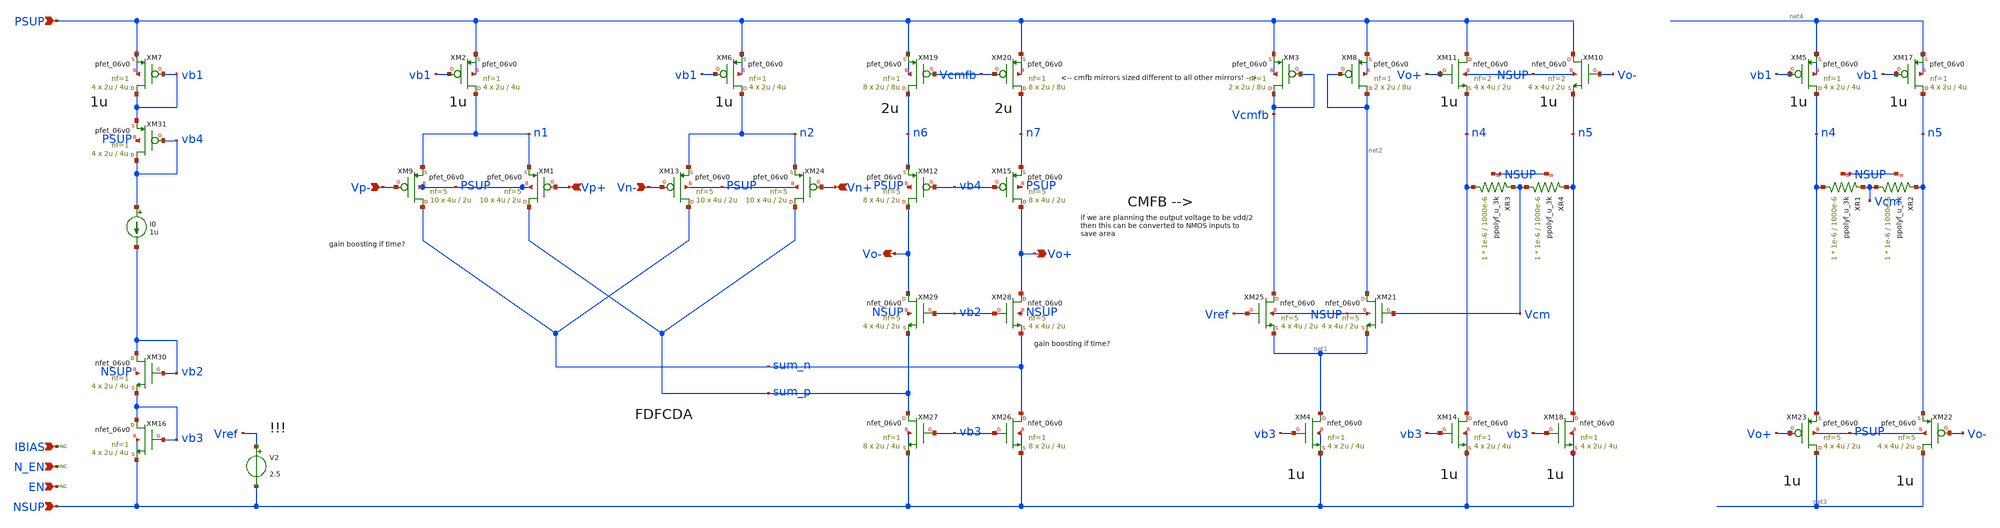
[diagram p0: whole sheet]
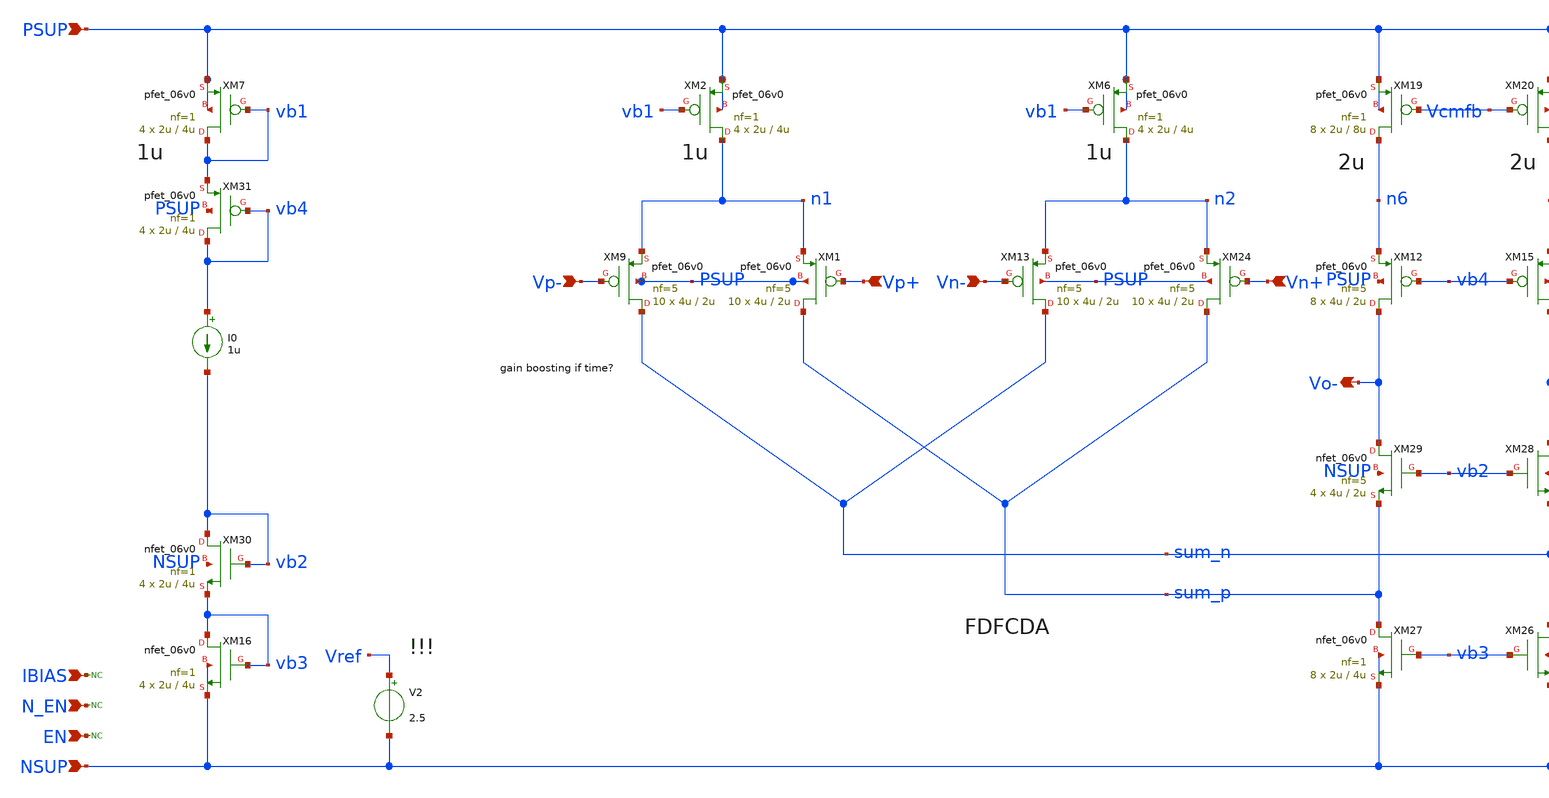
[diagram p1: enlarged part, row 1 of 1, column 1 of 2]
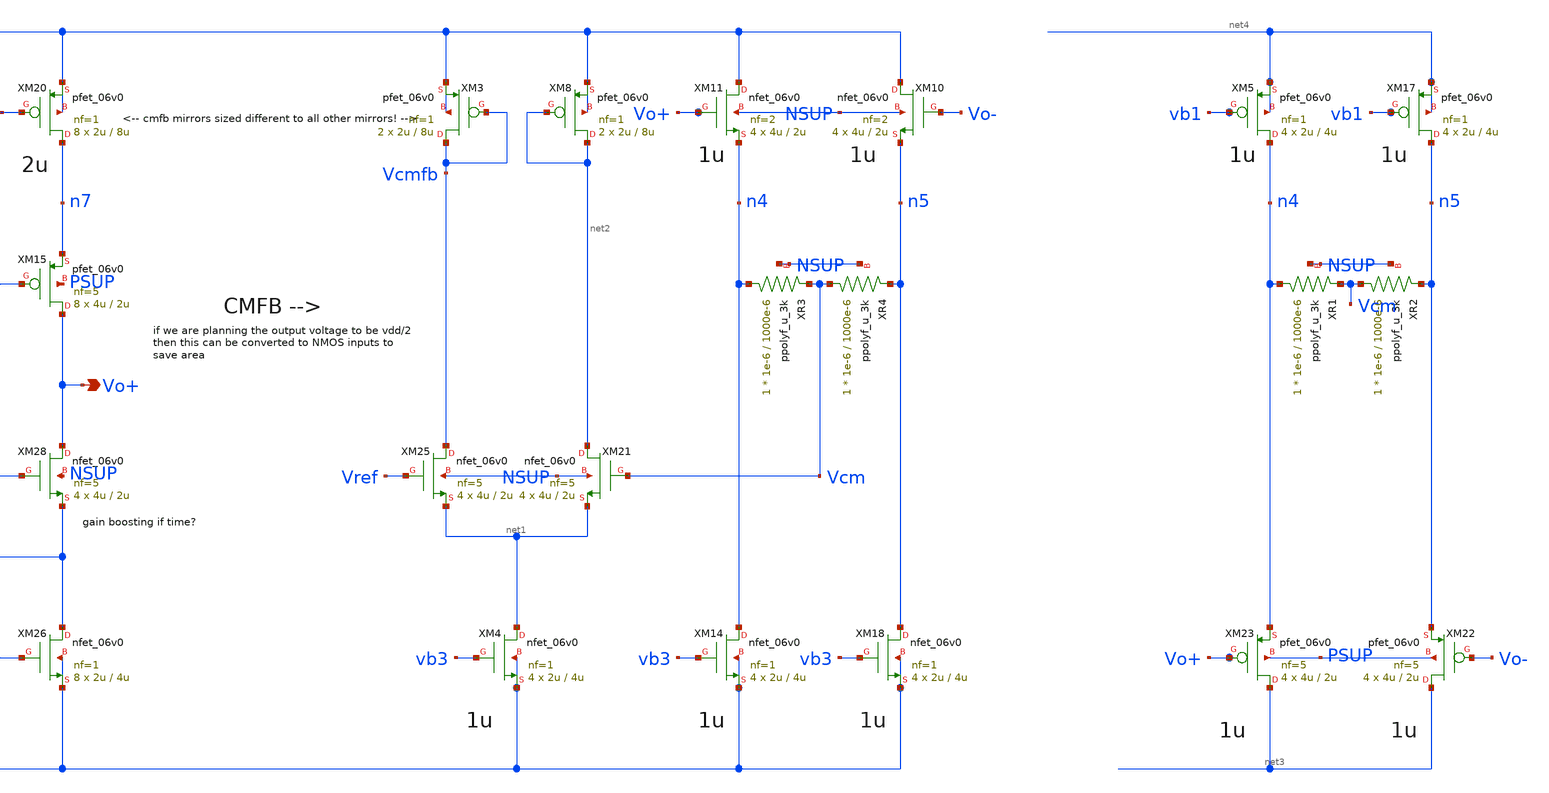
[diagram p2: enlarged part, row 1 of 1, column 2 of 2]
** sch_path: xschem/blocks/fdda/junk/fdda_copyjustincasseeee.sch
**.subckt fdda_copyjustincasseeee PSUP NSUP N_EN EN IBIAS Vp+ Vp- Vn+ Vn- Vo- Vo+
*.ipin PSUP
*.ipin NSUP
*.ipin N_EN
*.ipin EN
*.ipin IBIAS
*.ipin Vp+
*.ipin Vp-
*.ipin Vn+
*.ipin Vn-
*.opin Vo-
*.opin Vo+
* noconn N_EN
* noconn EN
I0 vb4 vb2 1u
XM7 vb1 vb1 PSUP PSUP pfet_06v0 L=4u W=2u nf=1 ad='int((nf+1)/2) * W/nf * 0.18u' as='int((nf+2)/2) * W/nf * 0.18u'
+ pd='2*int((nf+1)/2) * (W/nf + 0.18u)' ps='2*int((nf+2)/2) * (W/nf + 0.18u)' nrd='0.18u / W' nrs='0.18u / W'
+ sa=0 sb=0 sd=0 m=4
* noconn IBIAS
XM16 vb3 vb3 NSUP NSUP nfet_06v0 L=4u W=2u nf=1 ad='int((nf+1)/2) * W/nf * 0.18u' as='int((nf+2)/2) * W/nf * 0.18u'
+ pd='2*int((nf+1)/2) * (W/nf + 0.18u)' ps='2*int((nf+2)/2) * (W/nf + 0.18u)' nrd='0.18u / W' nrs='0.18u / W'
+ sa=0 sb=0 sd=0 m=4
V2 Vref NSUP 2.5
XM9 sum_n Vp- n1 PSUP pfet_06v0 L=2u W=4u nf=5 ad='int((nf+1)/2) * W/nf * 0.18u' as='int((nf+2)/2) * W/nf * 0.18u'
+ pd='2*int((nf+1)/2) * (W/nf + 0.18u)' ps='2*int((nf+2)/2) * (W/nf + 0.18u)' nrd='0.18u / W' nrs='0.18u / W'
+ sa=0 sb=0 sd=0 m=10
XM1 sum_p Vp+ n1 PSUP pfet_06v0 L=2u W=4u nf=5 ad='int((nf+1)/2) * W/nf * 0.18u' as='int((nf+2)/2) * W/nf * 0.18u'
+ pd='2*int((nf+1)/2) * (W/nf + 0.18u)' ps='2*int((nf+2)/2) * (W/nf + 0.18u)' nrd='0.18u / W' nrs='0.18u / W'
+ sa=0 sb=0 sd=0 m=10
XM2 n1 vb1 PSUP PSUP pfet_06v0 L=4u W=2u nf=1 ad='int((nf+1)/2) * W/nf * 0.18u' as='int((nf+2)/2) * W/nf * 0.18u'
+ pd='2*int((nf+1)/2) * (W/nf + 0.18u)' ps='2*int((nf+2)/2) * (W/nf + 0.18u)' nrd='0.18u / W' nrs='0.18u / W'
+ sa=0 sb=0 sd=0 m=4
XM6 n2 vb1 PSUP PSUP pfet_06v0 L=4u W=2u nf=1 ad='int((nf+1)/2) * W/nf * 0.18u' as='int((nf+2)/2) * W/nf * 0.18u'
+ pd='2*int((nf+1)/2) * (W/nf + 0.18u)' ps='2*int((nf+2)/2) * (W/nf + 0.18u)' nrd='0.18u / W' nrs='0.18u / W'
+ sa=0 sb=0 sd=0 m=4
XM24 sum_p Vn+ n2 PSUP pfet_06v0 L=2u W=4u nf=5 ad='int((nf+1)/2) * W/nf * 0.18u' as='int((nf+2)/2) * W/nf * 0.18u'
+ pd='2*int((nf+1)/2) * (W/nf + 0.18u)' ps='2*int((nf+2)/2) * (W/nf + 0.18u)' nrd='0.18u / W' nrs='0.18u / W'
+ sa=0 sb=0 sd=0 m=10
XR3 n4 Vcm NSUP ppolyf_u_3k r_width=1e-6 r_length=1000e-6 m=1
XR4 Vcm n5 NSUP ppolyf_u_3k r_width=1e-6 r_length=1000e-6 m=1
XM13 sum_n Vn- n2 PSUP pfet_06v0 L=2u W=4u nf=5 ad='int((nf+1)/2) * W/nf * 0.18u' as='int((nf+2)/2) * W/nf * 0.18u'
+ pd='2*int((nf+1)/2) * (W/nf + 0.18u)' ps='2*int((nf+2)/2) * (W/nf + 0.18u)' nrd='0.18u / W' nrs='0.18u / W'
+ sa=0 sb=0 sd=0 m=10
XM12 Vo- vb4 n6 PSUP pfet_06v0 L=2u W=4u nf=5 ad='int((nf+1)/2) * W/nf * 0.18u' as='int((nf+2)/2) * W/nf * 0.18u'
+ pd='2*int((nf+1)/2) * (W/nf + 0.18u)' ps='2*int((nf+2)/2) * (W/nf + 0.18u)' nrd='0.18u / W' nrs='0.18u / W'
+ sa=0 sb=0 sd=0 m=8
XM15 Vo+ vb4 n7 PSUP pfet_06v0 L=2u W=4u nf=5 ad='int((nf+1)/2) * W/nf * 0.18u' as='int((nf+2)/2) * W/nf * 0.18u'
+ pd='2*int((nf+1)/2) * (W/nf + 0.18u)' ps='2*int((nf+2)/2) * (W/nf + 0.18u)' nrd='0.18u / W' nrs='0.18u / W'
+ sa=0 sb=0 sd=0 m=8
XM19 n6 Vcmfb PSUP PSUP pfet_06v0 L=8u W=2u nf=1 ad='int((nf+1)/2) * W/nf * 0.18u' as='int((nf+2)/2) * W/nf * 0.18u'
+ pd='2*int((nf+1)/2) * (W/nf + 0.18u)' ps='2*int((nf+2)/2) * (W/nf + 0.18u)' nrd='0.18u / W' nrs='0.18u / W'
+ sa=0 sb=0 sd=0 m=8
XM20 n7 Vcmfb PSUP PSUP pfet_06v0 L=8u W=2u nf=1 ad='int((nf+1)/2) * W/nf * 0.18u' as='int((nf+2)/2) * W/nf * 0.18u'
+ pd='2*int((nf+1)/2) * (W/nf + 0.18u)' ps='2*int((nf+2)/2) * (W/nf + 0.18u)' nrd='0.18u / W' nrs='0.18u / W'
+ sa=0 sb=0 sd=0 m=8
XM26 sum_n vb3 NSUP NSUP nfet_06v0 L=4u W=2u nf=1 ad='int((nf+1)/2) * W/nf * 0.18u' as='int((nf+2)/2) * W/nf * 0.18u'
+ pd='2*int((nf+1)/2) * (W/nf + 0.18u)' ps='2*int((nf+2)/2) * (W/nf + 0.18u)' nrd='0.18u / W' nrs='0.18u / W'
+ sa=0 sb=0 sd=0 m=8
XM27 sum_p vb3 NSUP NSUP nfet_06v0 L=4u W=2u nf=1 ad='int((nf+1)/2) * W/nf * 0.18u' as='int((nf+2)/2) * W/nf * 0.18u'
+ pd='2*int((nf+1)/2) * (W/nf + 0.18u)' ps='2*int((nf+2)/2) * (W/nf + 0.18u)' nrd='0.18u / W' nrs='0.18u / W'
+ sa=0 sb=0 sd=0 m=8
XM28 Vo+ vb2 sum_n NSUP nfet_06v0 L=2u W=4u nf=5 ad='int((nf+1)/2) * W/nf * 0.18u' as='int((nf+2)/2) * W/nf * 0.18u'
+ pd='2*int((nf+1)/2) * (W/nf + 0.18u)' ps='2*int((nf+2)/2) * (W/nf + 0.18u)' nrd='0.18u / W' nrs='0.18u / W'
+ sa=0 sb=0 sd=0 m=4
XM29 Vo- vb2 sum_p NSUP nfet_06v0 L=2u W=4u nf=5 ad='int((nf+1)/2) * W/nf * 0.18u' as='int((nf+2)/2) * W/nf * 0.18u'
+ pd='2*int((nf+1)/2) * (W/nf + 0.18u)' ps='2*int((nf+2)/2) * (W/nf + 0.18u)' nrd='0.18u / W' nrs='0.18u / W'
+ sa=0 sb=0 sd=0 m=4
XM30 vb2 vb2 vb3 NSUP nfet_06v0 L=4u W=2u nf=1 ad='int((nf+1)/2) * W/nf * 0.18u' as='int((nf+2)/2) * W/nf * 0.18u'
+ pd='2*int((nf+1)/2) * (W/nf + 0.18u)' ps='2*int((nf+2)/2) * (W/nf + 0.18u)' nrd='0.18u / W' nrs='0.18u / W'
+ sa=0 sb=0 sd=0 m=4
XM31 vb4 vb4 vb1 PSUP pfet_06v0 L=4u W=2u nf=1 ad='int((nf+1)/2) * W/nf * 0.18u' as='int((nf+2)/2) * W/nf * 0.18u'
+ pd='2*int((nf+1)/2) * (W/nf + 0.18u)' ps='2*int((nf+2)/2) * (W/nf + 0.18u)' nrd='0.18u / W' nrs='0.18u / W'
+ sa=0 sb=0 sd=0 m=4
XM3 Vcmfb Vcmfb PSUP PSUP pfet_06v0 L=8u W=2u nf=1 ad='int((nf+1)/2) * W/nf * 0.18u' as='int((nf+2)/2) * W/nf * 0.18u'
+ pd='2*int((nf+1)/2) * (W/nf + 0.18u)' ps='2*int((nf+2)/2) * (W/nf + 0.18u)' nrd='0.18u / W' nrs='0.18u / W'
+ sa=0 sb=0 sd=0 m=2
XM8 net2 net2 PSUP PSUP pfet_06v0 L=8u W=2u nf=1 ad='int((nf+1)/2) * W/nf * 0.18u' as='int((nf+2)/2) * W/nf * 0.18u'
+ pd='2*int((nf+1)/2) * (W/nf + 0.18u)' ps='2*int((nf+2)/2) * (W/nf + 0.18u)' nrd='0.18u / W' nrs='0.18u / W'
+ sa=0 sb=0 sd=0 m=2
XM21 net2 Vcm net1 NSUP nfet_06v0 L=2u W=4u nf=5 ad='int((nf+1)/2) * W/nf * 0.18u' as='int((nf+2)/2) * W/nf * 0.18u'
+ pd='2*int((nf+1)/2) * (W/nf + 0.18u)' ps='2*int((nf+2)/2) * (W/nf + 0.18u)' nrd='0.18u / W' nrs='0.18u / W'
+ sa=0 sb=0 sd=0 m=4
XM25 Vcmfb Vref net1 NSUP nfet_06v0 L=2u W=4u nf=5 ad='int((nf+1)/2) * W/nf * 0.18u' as='int((nf+2)/2) * W/nf * 0.18u'
+ pd='2*int((nf+1)/2) * (W/nf + 0.18u)' ps='2*int((nf+2)/2) * (W/nf + 0.18u)' nrd='0.18u / W' nrs='0.18u / W'
+ sa=0 sb=0 sd=0 m=4
XM4 net1 vb3 NSUP NSUP nfet_06v0 L=4u W=2u nf=1 ad='int((nf+1)/2) * W/nf * 0.18u' as='int((nf+2)/2) * W/nf * 0.18u'
+ pd='2*int((nf+1)/2) * (W/nf + 0.18u)' ps='2*int((nf+2)/2) * (W/nf + 0.18u)' nrd='0.18u / W' nrs='0.18u / W'
+ sa=0 sb=0 sd=0 m=4
XM14 n4 vb3 NSUP NSUP nfet_06v0 L=4u W=2u nf=1 ad='int((nf+1)/2) * W/nf * 0.18u' as='int((nf+2)/2) * W/nf * 0.18u'
+ pd='2*int((nf+1)/2) * (W/nf + 0.18u)' ps='2*int((nf+2)/2) * (W/nf + 0.18u)' nrd='0.18u / W' nrs='0.18u / W'
+ sa=0 sb=0 sd=0 m=4
XM18 n5 vb3 NSUP NSUP nfet_06v0 L=4u W=2u nf=1 ad='int((nf+1)/2) * W/nf * 0.18u' as='int((nf+2)/2) * W/nf * 0.18u'
+ pd='2*int((nf+1)/2) * (W/nf + 0.18u)' ps='2*int((nf+2)/2) * (W/nf + 0.18u)' nrd='0.18u / W' nrs='0.18u / W'
+ sa=0 sb=0 sd=0 m=4
XM10 PSUP Vo- n5 NSUP nfet_06v0 L=2u W=4u nf=2 ad='int((nf+1)/2) * W/nf * 0.18u' as='int((nf+2)/2) * W/nf * 0.18u'
+ pd='2*int((nf+1)/2) * (W/nf + 0.18u)' ps='2*int((nf+2)/2) * (W/nf + 0.18u)' nrd='0.18u / W' nrs='0.18u / W'
+ sa=0 sb=0 sd=0 m=4
XM11 PSUP Vo+ n4 NSUP nfet_06v0 L=2u W=4u nf=2 ad='int((nf+1)/2) * W/nf * 0.18u' as='int((nf+2)/2) * W/nf * 0.18u'
+ pd='2*int((nf+1)/2) * (W/nf + 0.18u)' ps='2*int((nf+2)/2) * (W/nf + 0.18u)' nrd='0.18u / W' nrs='0.18u / W'
+ sa=0 sb=0 sd=0 m=4
XM22 net3 Vo- n5 PSUP pfet_06v0 L=2u W=4u nf=5 ad='int((nf+1)/2) * W/nf * 0.18u' as='int((nf+2)/2) * W/nf * 0.18u'
+ pd='2*int((nf+1)/2) * (W/nf + 0.18u)' ps='2*int((nf+2)/2) * (W/nf + 0.18u)' nrd='0.18u / W' nrs='0.18u / W'
+ sa=0 sb=0 sd=0 m=4
XM23 net3 Vo+ n4 PSUP pfet_06v0 L=2u W=4u nf=5 ad='int((nf+1)/2) * W/nf * 0.18u' as='int((nf+2)/2) * W/nf * 0.18u'
+ pd='2*int((nf+1)/2) * (W/nf + 0.18u)' ps='2*int((nf+2)/2) * (W/nf + 0.18u)' nrd='0.18u / W' nrs='0.18u / W'
+ sa=0 sb=0 sd=0 m=4
XR1 n4 Vcm NSUP ppolyf_u_3k r_width=1e-6 r_length=1000e-6 m=1
XR2 Vcm n5 NSUP ppolyf_u_3k r_width=1e-6 r_length=1000e-6 m=1
XM5 n4 vb1 net4 net4 pfet_06v0 L=4u W=2u nf=1 ad='int((nf+1)/2) * W/nf * 0.18u' as='int((nf+2)/2) * W/nf * 0.18u'
+ pd='2*int((nf+1)/2) * (W/nf + 0.18u)' ps='2*int((nf+2)/2) * (W/nf + 0.18u)' nrd='0.18u / W' nrs='0.18u / W'
+ sa=0 sb=0 sd=0 m=4
XM17 n5 vb1 net4 net4 pfet_06v0 L=4u W=2u nf=1 ad='int((nf+1)/2) * W/nf * 0.18u' as='int((nf+2)/2) * W/nf * 0.18u'
+ pd='2*int((nf+1)/2) * (W/nf + 0.18u)' ps='2*int((nf+2)/2) * (W/nf + 0.18u)' nrd='0.18u / W' nrs='0.18u / W'
+ sa=0 sb=0 sd=0 m=4
**.ends
.end
